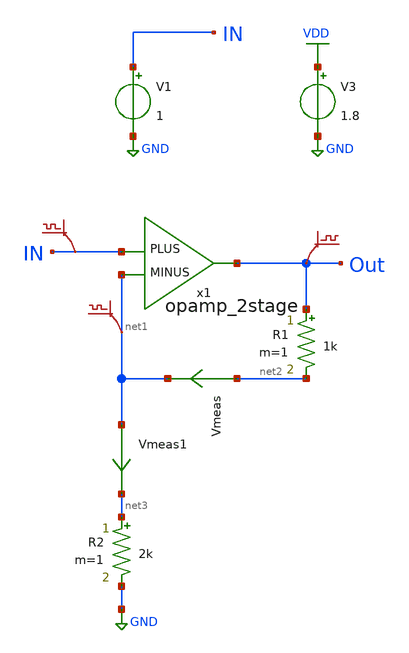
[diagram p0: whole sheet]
** sch_path: lib/xschem/LDO/test_opamp.sch
**.subckt test_opamp
R1 Out net2 1k m=1
V1 IN GND 1
V3 VDD GND 1.8
.save v(in)
x1 net1 IN Out opamp_2stage
R2 net3 GND 2k m=1
.save v(out)
.save v(net1)
Vmeas net2 net1 0
.save i(vmeas)
Vmeas1 net1 net3 0
.save i(vmeas1)
**** begin user architecture code

.lib $::SKYWATER_MODELS/sky130.lib.spice tt


**** end user architecture code
**.ends

* expanding   symbol:  LDO/opamp_2stage.sym # of pins=3
** sym_path: lib/xschem/LDO/opamp_2stage.sym
** sch_path: lib/xschem/LDO/opamp_2stage.sch
.subckt opamp_2stage MINUS PLUS Vout
*.ipin PLUS
*.ipin MINUS
*.opin Vout
XM8 net1 net1 net6 VDD sky130_fd_pr__pfet_01v8 L=0.15 W=1 nf=1 ad='int((nf+1)/2) * W/nf * 0.29' as='int((nf+2)/2) * W/nf * 0.29'
+ pd='2*int((nf+1)/2) * (W/nf + 0.29)' ps='2*int((nf+2)/2) * (W/nf + 0.29)' nrd='0.29 / W' nrs='0.29 / W'
+ sa=0 sb=0 sd=0 mult=1 m=1
XM9 net7 net2 net3 GND sky130_fd_pr__nfet_01v8 L=0.15 W=1 nf=1 ad='int((nf+1)/2) * W/nf * 0.29' as='int((nf+2)/2) * W/nf * 0.29'
+ pd='2*int((nf+1)/2) * (W/nf + 0.29)' ps='2*int((nf+2)/2) * (W/nf + 0.29)' nrd='0.29 / W' nrs='0.29 / W'
+ sa=0 sb=0 sd=0 mult=1 m=1
XM1 Vcs net1 net6 VDD sky130_fd_pr__pfet_01v8 L=0.15 W=1 nf=1 ad='int((nf+1)/2) * W/nf * 0.29' as='int((nf+2)/2) * W/nf * 0.29'
+ pd='2*int((nf+1)/2) * (W/nf + 0.29)' ps='2*int((nf+2)/2) * (W/nf + 0.29)' nrd='0.29 / W' nrs='0.29 / W'
+ sa=0 sb=0 sd=0 mult=1 m=1
XM2 net1 Vcs net7 GND sky130_fd_pr__nfet_01v8 L=0.15 W=1 nf=1 ad='int((nf+1)/2) * W/nf * 0.29' as='int((nf+2)/2) * W/nf * 0.29'
+ pd='2*int((nf+1)/2) * (W/nf + 0.29)' ps='2*int((nf+2)/2) * (W/nf + 0.29)' nrd='0.29 / W' nrs='0.29 / W'
+ sa=0 sb=0 sd=0 mult=1 m=1
XM3 Vcs Vcs net5 GND sky130_fd_pr__nfet_01v8 L=0.15 W=1 nf=1 ad='int((nf+1)/2) * W/nf * 0.29' as='int((nf+2)/2) * W/nf * 0.29'
+ pd='2*int((nf+1)/2) * (W/nf + 0.29)' ps='2*int((nf+2)/2) * (W/nf + 0.29)' nrd='0.29 / W' nrs='0.29 / W'
+ sa=0 sb=0 sd=0 mult=1 m=1
XM4 net2 net2 GND GND sky130_fd_pr__nfet_01v8 L=0.15 W=1 nf=1 ad='int((nf+1)/2) * W/nf * 0.29' as='int((nf+2)/2) * W/nf * 0.29'
+ pd='2*int((nf+1)/2) * (W/nf + 0.29)' ps='2*int((nf+2)/2) * (W/nf + 0.29)' nrd='0.29 / W' nrs='0.29 / W'
+ sa=0 sb=0 sd=0 mult=1 m=1
R1 net4 GND 500 m=1
C3 net12 Vout 2p m=1
XM6 net10 net10 GND GND sky130_fd_pr__nfet_01v8 L=0.15 W=2 nf=1 ad='int((nf+1)/2) * W/nf * 0.29' as='int((nf+2)/2) * W/nf * 0.29'
+ pd='2*int((nf+1)/2) * (W/nf + 0.29)' ps='2*int((nf+2)/2) * (W/nf + 0.29)' nrd='0.29 / W' nrs='0.29 / W'
+ sa=0 sb=0 sd=0 mult=1 m=1
XM5 net14 net10 GND GND sky130_fd_pr__nfet_01v8 L=0.15 W=2 nf=1 ad='int((nf+1)/2) * W/nf * 0.29' as='int((nf+2)/2) * W/nf * 0.29'
+ pd='2*int((nf+1)/2) * (W/nf + 0.29)' ps='2*int((nf+2)/2) * (W/nf + 0.29)' nrd='0.29 / W' nrs='0.29 / W'
+ sa=0 sb=0 sd=0 mult=1 m=1
XM7 net9 PLUS net8 VDD sky130_fd_pr__pfet_01v8 L=0.15 W=5 nf=1 ad='int((nf+1)/2) * W/nf * 0.29' as='int((nf+2)/2) * W/nf * 0.29'
+ pd='2*int((nf+1)/2) * (W/nf + 0.29)' ps='2*int((nf+2)/2) * (W/nf + 0.29)' nrd='0.29 / W' nrs='0.29 / W'
+ sa=0 sb=0 sd=0 mult=1 m=1
XM10 net11 MINUS net8 VDD sky130_fd_pr__pfet_01v8 L=0.15 W=5 nf=1 ad='int((nf+1)/2) * W/nf * 0.29' as='int((nf+2)/2) * W/nf * 0.29'
+ pd='2*int((nf+1)/2) * (W/nf + 0.29)' ps='2*int((nf+2)/2) * (W/nf + 0.29)' nrd='0.29 / W' nrs='0.29 / W'
+ sa=0 sb=0 sd=0 mult=1 m=1
XM11 net8 net1 VDD VDD sky130_fd_pr__pfet_01v8 L=0.15 W=5 nf=1 ad='int((nf+1)/2) * W/nf * 0.29' as='int((nf+2)/2) * W/nf * 0.29'
+ pd='2*int((nf+1)/2) * (W/nf + 0.29)' ps='2*int((nf+2)/2) * (W/nf + 0.29)' nrd='0.29 / W' nrs='0.29 / W'
+ sa=0 sb=0 sd=0 mult=1 m=1
XM13 Vout net9 GND GND sky130_fd_pr__nfet_01v8 L=0.15 W=5 nf=1 ad='int((nf+1)/2) * W/nf * 0.29' as='int((nf+2)/2) * W/nf * 0.29'
+ pd='2*int((nf+1)/2) * (W/nf + 0.29)' ps='2*int((nf+2)/2) * (W/nf + 0.29)' nrd='0.29 / W' nrs='0.29 / W'
+ sa=0 sb=0 sd=0 mult=1 m=1
XM16 net13 net1 VDD VDD sky130_fd_pr__pfet_01v8 L=0.15 W=5 nf=1 ad='int((nf+1)/2) * W/nf * 0.29' as='int((nf+2)/2) * W/nf * 0.29'
+ pd='2*int((nf+1)/2) * (W/nf + 0.29)' ps='2*int((nf+2)/2) * (W/nf + 0.29)' nrd='0.29 / W' nrs='0.29 / W'
+ sa=0 sb=0 sd=0 mult=1 m=1
.save v(plus)
.save v(minus)
.save v(net1)
.save v(net9)
.save v(net11)
Vmeas net3 net4 0
.save i(vmeas)
.save v(minus)
.save v(vout)
.save v(plus)
.save v(net6)
.save v(net4)
Vmeas1 net11 net10 0
.save i(vmeas1)
Vmeas2 net9 net14 0
.save i(vmeas2)
Vmeas3 net13 Vout 0
.save i(vmeas3)
Vmeas4 net5 net2 0
.save i(vmeas4)
.save v(net2)
.save v(net7)
.save v(vcs)
XM12 net12 Vcs net9 GND sky130_fd_pr__nfet_01v8 L=0.15 W=2 nf=1 ad='int((nf+1)/2) * W/nf * 0.29' as='int((nf+2)/2) * W/nf * 0.29'
+ pd='2*int((nf+1)/2) * (W/nf + 0.29)' ps='2*int((nf+2)/2) * (W/nf + 0.29)' nrd='0.29 / W' nrs='0.29 / W'
+ sa=0 sb=0 sd=0 mult=1 m=1
I0 VDD net6 0.25u
.ends

.GLOBAL GND
.GLOBAL VDD
**** begin user architecture code


.control
save all
op
write test_opamp.raw
.endc


**** end user architecture code
.end
